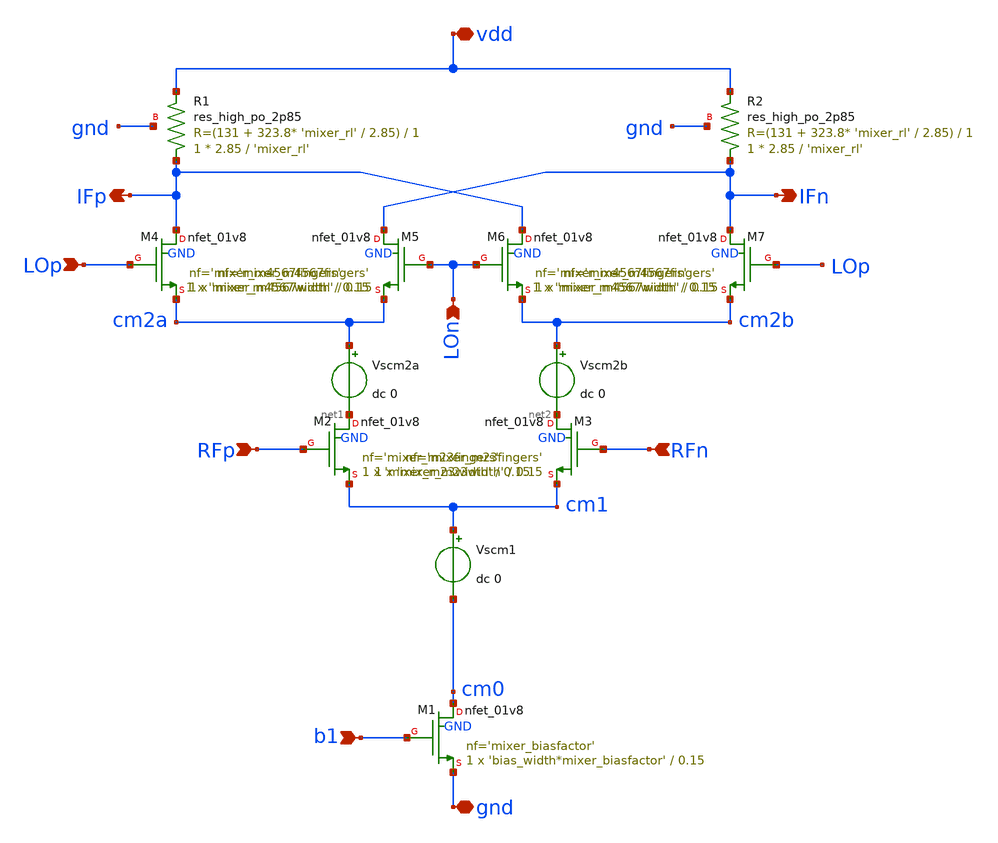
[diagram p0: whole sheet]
** sch_path: xschem/mixer_param.sch
**.subckt mixer_param LOp RFp RFn LOn b1 gnd vdd IFp IFn
*.ipin LOp
*.ipin RFp
*.ipin RFn
*.ipin LOn
*.ipin b1
*.iopin gnd
*.iopin vdd
*.opin IFp
*.opin IFn
XM2 net1 RFp cm1 GND sky130_fd_pr__nfet_01v8 L=0.15 W='mixer_m23width' nf='mixer_m23fingers' ad='int((nf+1)/2) * W/nf * 0.29'
+ as='int((nf+2)/2) * W/nf * 0.29' pd='2*int((nf+1)/2) * (W/nf + 0.29)' ps='2*int((nf+2)/2) * (W/nf + 0.29)'
+ nrd='0.29 / W' nrs='0.29 / W' sa=0 sb=0 sd=0 mult=1 m=1
XM1 cm0 b1 gnd GND sky130_fd_pr__nfet_01v8 L=0.15 W='bias_width*mixer_biasfactor' nf='mixer_biasfactor'
+ ad='int((nf+1)/2) * W/nf * 0.29' as='int((nf+2)/2) * W/nf * 0.29' pd='2*int((nf+1)/2) * (W/nf + 0.29)'
+ ps='2*int((nf+2)/2) * (W/nf + 0.29)' nrd='0.29 / W' nrs='0.29 / W' sa=0 sb=0 sd=0 mult=1 m=1
XM3 net2 RFn cm1 GND sky130_fd_pr__nfet_01v8 L=0.15 W='mixer_m23width' nf='mixer_m23fingers' ad='int((nf+1)/2) * W/nf * 0.29'
+ as='int((nf+2)/2) * W/nf * 0.29' pd='2*int((nf+1)/2) * (W/nf + 0.29)' ps='2*int((nf+2)/2) * (W/nf + 0.29)'
+ nrd='0.29 / W' nrs='0.29 / W' sa=0 sb=0 sd=0 mult=1 m=1
XM4 IFp LOp cm2a GND sky130_fd_pr__nfet_01v8 L=0.15 W='mixer_m4567width' nf='mixer_m4567fingers' ad='int((nf+1)/2) * W/nf * 0.29'
+ as='int((nf+2)/2) * W/nf * 0.29' pd='2*int((nf+1)/2) * (W/nf + 0.29)' ps='2*int((nf+2)/2) * (W/nf + 0.29)'
+ nrd='0.29 / W' nrs='0.29 / W' sa=0 sb=0 sd=0 mult=1 m=1
XM5 IFn LOn cm2a GND sky130_fd_pr__nfet_01v8 L=0.15 W='mixer_m4567width' nf='mixer_m4567fingers' ad='int((nf+1)/2) * W/nf * 0.29'
+ as='int((nf+2)/2) * W/nf * 0.29' pd='2*int((nf+1)/2) * (W/nf + 0.29)' ps='2*int((nf+2)/2) * (W/nf + 0.29)'
+ nrd='0.29 / W' nrs='0.29 / W' sa=0 sb=0 sd=0 mult=1 m=1
XM6 IFp LOn cm2b GND sky130_fd_pr__nfet_01v8 L=0.15 W='mixer_m4567width' nf='mixer_m4567fingers' ad='int((nf+1)/2) * W/nf * 0.29'
+ as='int((nf+2)/2) * W/nf * 0.29' pd='2*int((nf+1)/2) * (W/nf + 0.29)' ps='2*int((nf+2)/2) * (W/nf + 0.29)'
+ nrd='0.29 / W' nrs='0.29 / W' sa=0 sb=0 sd=0 mult=1 m=1
XM7 IFn LOp cm2b GND sky130_fd_pr__nfet_01v8 L=0.15 W='mixer_m4567width' nf='mixer_m4567fingers' ad='int((nf+1)/2) * W/nf * 0.29'
+ as='int((nf+2)/2) * W/nf * 0.29' pd='2*int((nf+1)/2) * (W/nf + 0.29)' ps='2*int((nf+2)/2) * (W/nf + 0.29)'
+ nrd='0.29 / W' nrs='0.29 / W' sa=0 sb=0 sd=0 mult=1 m=1
Vscm1 cm1 cm0 dc 0
Vscm2b cm2b net2 dc 0
Vscm2a cm2a net1 dc 0
XR1 IFp vdd gnd sky130_fd_pr__res_high_po_2p85 L='mixer_rl' mult=1 m=1
XR2 IFn vdd gnd sky130_fd_pr__res_high_po_2p85 L='mixer_rl' mult=1 m=1
**.ends
.end
